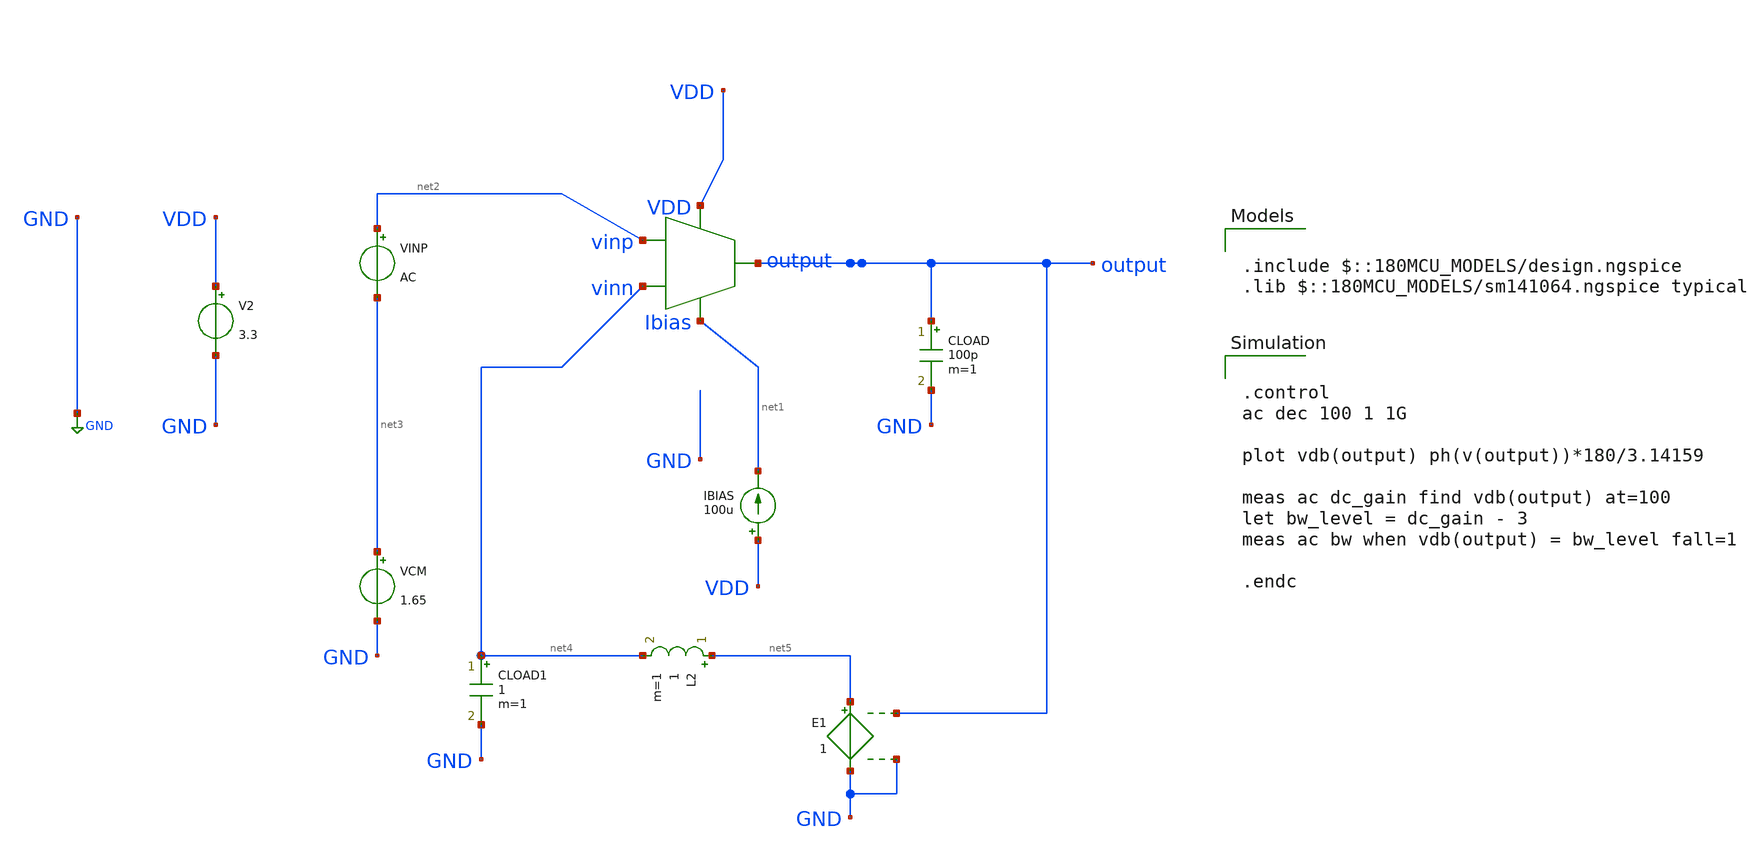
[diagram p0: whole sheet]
** sch_path: designs/libs/core_amps/ota_telescopic/telescopic_ac_open_tb.sch
**.subckt telescopic_ac_open_tb
IBIAS VDD net1 100u
V2 VDD GND 3.3
CLOAD output GND 100p m=1
VINP net2 net3 AC
VCM net3 GND 1.65
L2 net5 net4 1 m=1
CLOAD1 net4 GND 1 m=1
E1 net5 GND output GND 1
X1 net2 net4 VDD net1 output telescopic_cascode
**** begin user architecture code

.include $::180MCU_MODELS/design.ngspice
.lib $::180MCU_MODELS/sm141064.ngspice typical



.control
ac dec 100 1 1G

plot vdb(output) ph(v(output))*180/3.14159

meas ac dc_gain find vdb(output) at=100
let bw_level = dc_gain - 3
meas ac bw when vdb(output) = bw_level fall=1

.endc



**** end user architecture code
**.ends

* expanding   symbol:  libs/core_amps/ota_telescopic/telescopic_cascode.sym # of pins=5
** sym_path: designs/libs/core_amps/ota_telescopic/telescopic_cascode.sym
** sch_path: designs/libs/core_amps/ota_telescopic/telescopic_cascode.sch
.subckt telescopic_cascode vinp vinn VDD Ibias output
*.ipin vinp
*.ipin vinn
*.opin output
*.iopin Ibias
*.iopin VDD
XM8 output net4 net3 VDD pfet_03v3 L=0.56u W=65u nf=1 ad='int((nf+1)/2) * W/nf * 0.18u' as='int((nf+2)/2) * W/nf * 0.18u'
+ pd='2*int((nf+1)/2) * (W/nf + 0.18u)' ps='2*int((nf+2)/2) * (W/nf + 0.18u)' nrd='0.18u / W' nrs='0.18u / W'
+ sa=0 sb=0 sd=0 m=4
XM4 output VBN1 net7 GND nfet_03v3 L=0.5u W=40u nf=1 ad='int((nf+1)/2) * W/nf * 0.18u' as='int((nf+2)/2) * W/nf * 0.18u'
+ pd='2*int((nf+1)/2) * (W/nf + 0.18u)' ps='2*int((nf+2)/2) * (W/nf + 0.18u)' nrd='0.18u / W' nrs='0.18u / W'
+ sa=0 sb=0 sd=0 m=1
XM1 net5 vinp net6 GND nfet_03v3 L=0.5u W=30u nf=1 ad='int((nf+1)/2) * W/nf * 0.18u' as='int((nf+2)/2) * W/nf * 0.18u'
+ pd='2*int((nf+1)/2) * (W/nf + 0.18u)' ps='2*int((nf+2)/2) * (W/nf + 0.18u)' nrd='0.18u / W' nrs='0.18u / W'
+ sa=0 sb=0 sd=0 m=1
XM2 net1 VBN1 net5 GND nfet_03v3 L=0.5u W=40u nf=1 ad='int((nf+1)/2) * W/nf * 0.18u' as='int((nf+2)/2) * W/nf * 0.18u'
+ pd='2*int((nf+1)/2) * (W/nf + 0.18u)' ps='2*int((nf+2)/2) * (W/nf + 0.18u)' nrd='0.18u / W' nrs='0.18u / W'
+ sa=0 sb=0 sd=0 m=1
XM3 net7 vinn net6 GND nfet_03v3 L=0.5u W=30u nf=1 ad='int((nf+1)/2) * W/nf * 0.18u' as='int((nf+2)/2) * W/nf * 0.18u'
+ pd='2*int((nf+1)/2) * (W/nf + 0.18u)' ps='2*int((nf+2)/2) * (W/nf + 0.18u)' nrd='0.18u / W' nrs='0.18u / W'
+ sa=0 sb=0 sd=0 m=1
XM5 net3 net1 VDD VDD pfet_03v3 L=0.56u W=65u nf=1 ad='int((nf+1)/2) * W/nf * 0.18u' as='int((nf+2)/2) * W/nf * 0.18u'
+ pd='2*int((nf+1)/2) * (W/nf + 0.18u)' ps='2*int((nf+2)/2) * (W/nf + 0.18u)' nrd='0.18u / W' nrs='0.18u / W'
+ sa=0 sb=0 sd=0 m=4
XM6 net1 net4 net2 VDD pfet_03v3 L=0.56u W=65u nf=1 ad='int((nf+1)/2) * W/nf * 0.18u' as='int((nf+2)/2) * W/nf * 0.18u'
+ pd='2*int((nf+1)/2) * (W/nf + 0.18u)' ps='2*int((nf+2)/2) * (W/nf + 0.18u)' nrd='0.18u / W' nrs='0.18u / W'
+ sa=0 sb=0 sd=0 m=4
XM7 net2 net1 VDD VDD pfet_03v3 L=0.56u W=65u nf=1 ad='int((nf+1)/2) * W/nf * 0.18u' as='int((nf+2)/2) * W/nf * 0.18u'
+ pd='2*int((nf+1)/2) * (W/nf + 0.18u)' ps='2*int((nf+2)/2) * (W/nf + 0.18u)' nrd='0.18u / W' nrs='0.18u / W'
+ sa=0 sb=0 sd=0 m=4
XM9 net6 Ibias GND GND nfet_03v3 L=0.28u W=15.54u nf=1 ad='int((nf+1)/2) * W/nf * 0.18u' as='int((nf+2)/2) * W/nf * 0.18u'
+ pd='2*int((nf+1)/2) * (W/nf + 0.18u)' ps='2*int((nf+2)/2) * (W/nf + 0.18u)' nrd='0.18u / W' nrs='0.18u / W'
+ sa=0 sb=0 sd=0 m=1
XM10 Ibias Ibias GND GND nfet_03v3 L=.28u W=5.18u nf=1 ad='int((nf+1)/2) * W/nf * 0.18u' as='int((nf+2)/2) * W/nf * 0.18u'
+ pd='2*int((nf+1)/2) * (W/nf + 0.18u)' ps='2*int((nf+2)/2) * (W/nf + 0.18u)' nrd='0.18u / W' nrs='0.18u / W'
+ sa=0 sb=0 sd=0 m=1
**** begin user architecture code


.include /foss/pdks/gf180mcuD/libs.tech/ngspice/design.ngspice
.lib /foss/pdks/gf180mcuD/libs.tech/ngspice/sm141064.ngspice typical

**** end user architecture code
V1 VBN1 GND 2.2
V2 net4 GND 1.6
.ends

.GLOBAL GND
.end
